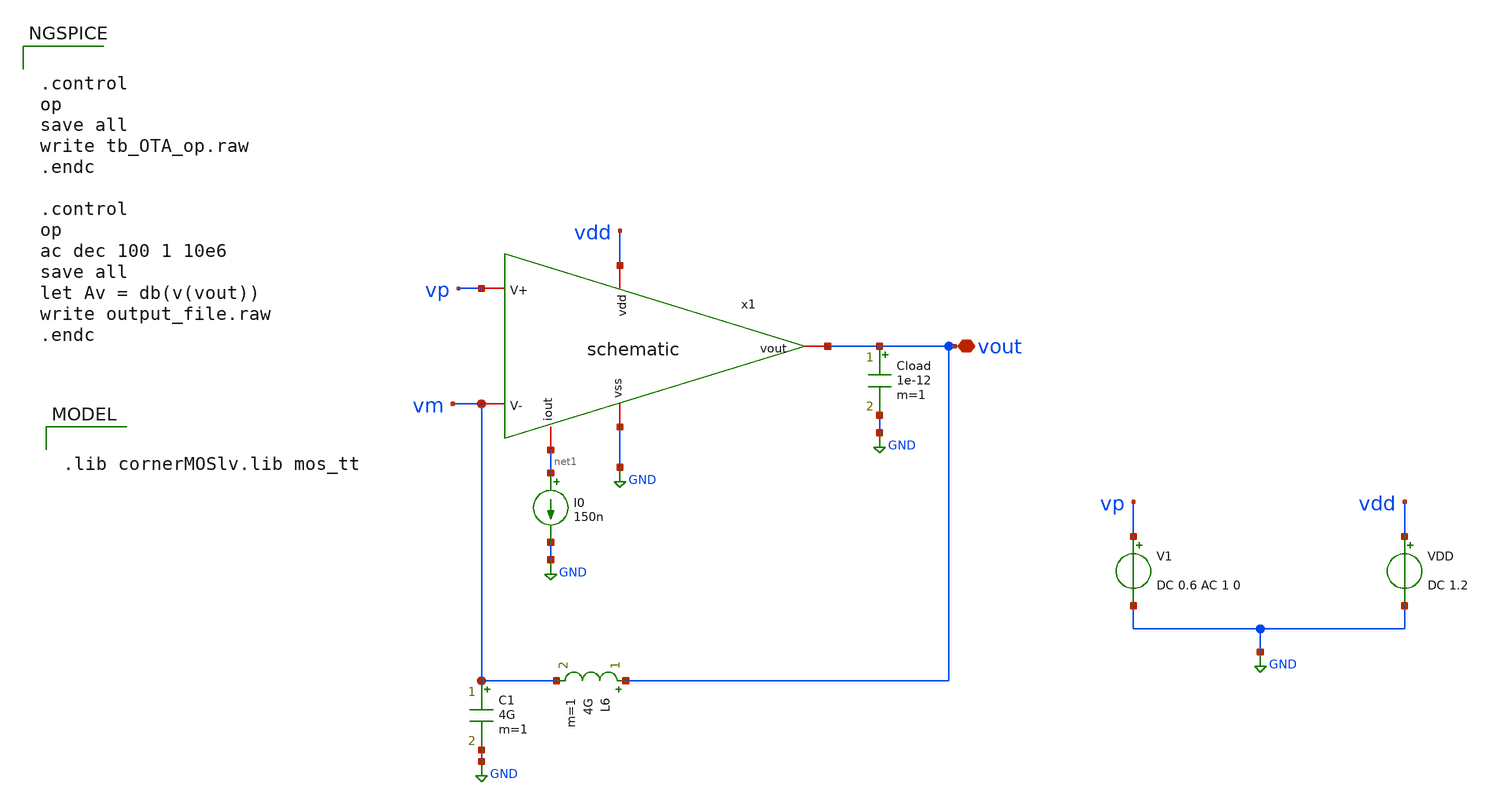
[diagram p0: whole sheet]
** sch_path: utils/gmid_demonstration/testbench/ota_testbench.sch
**.subckt ota_testbench vout
*.iopin vout
V1 vp GND DC 0.6 AC 1 0
VDD vdd GND DC 1.2
I0 net1 GND 150n
Cload vout GND 1e-12 m=1
L6 vout vm 4G m=1
C1 vm GND 4G m=1
x1 vdd net1 vm vp vout GND schematic
**** begin user architecture code

.lib cornerMOSlv.lib mos_tt



.control
op
save all
write tb_OTA_op.raw
.endc

.control
op
ac dec 100 1 10e6
save all
let Av = db(v(vout))
write output_file.raw
.endc


**** end user architecture code
**.ends

* expanding   symbol:  schematic.sym # of pins=6
** sym_path: utils/gmid_demonstration/testbench/schematic.sym
** sch_path: utils/gmid_demonstration/testbench/schematic.sch
.subckt schematic vdd iout V- V+ vout vss
*.iopin vdd
*.iopin iout
*.iopin vout
*.iopin vss
*.iopin V+
*.iopin V-
XM1 net2 V- net1 vdd sg13_lv_pmos w=1.25u l=5.20u ng=1 m=1 mm_ok=1
XM2 net2 net2 vss vss sg13_lv_nmos w=0.68u l=9.88u ng=1 m=1 mm_ok=1
XM3 vout V+ net1 vdd sg13_lv_pmos w=1.25u l=5.20u ng=1 m=1 mm_ok=1
XM4 vout net2 vss vss sg13_lv_nmos w=0.68u l=9.88u ng=1 m=1 mm_ok=1
XM5 net1 iout vdd vdd sg13_lv_pmos w=2u l=0.13u ng=1 m=1 mm_ok=1
XM7 iout iout vdd vdd sg13_lv_pmos w=2u l=0.13u ng=1 m=1 mm_ok=1
.ends

.GLOBAL GND
.end
